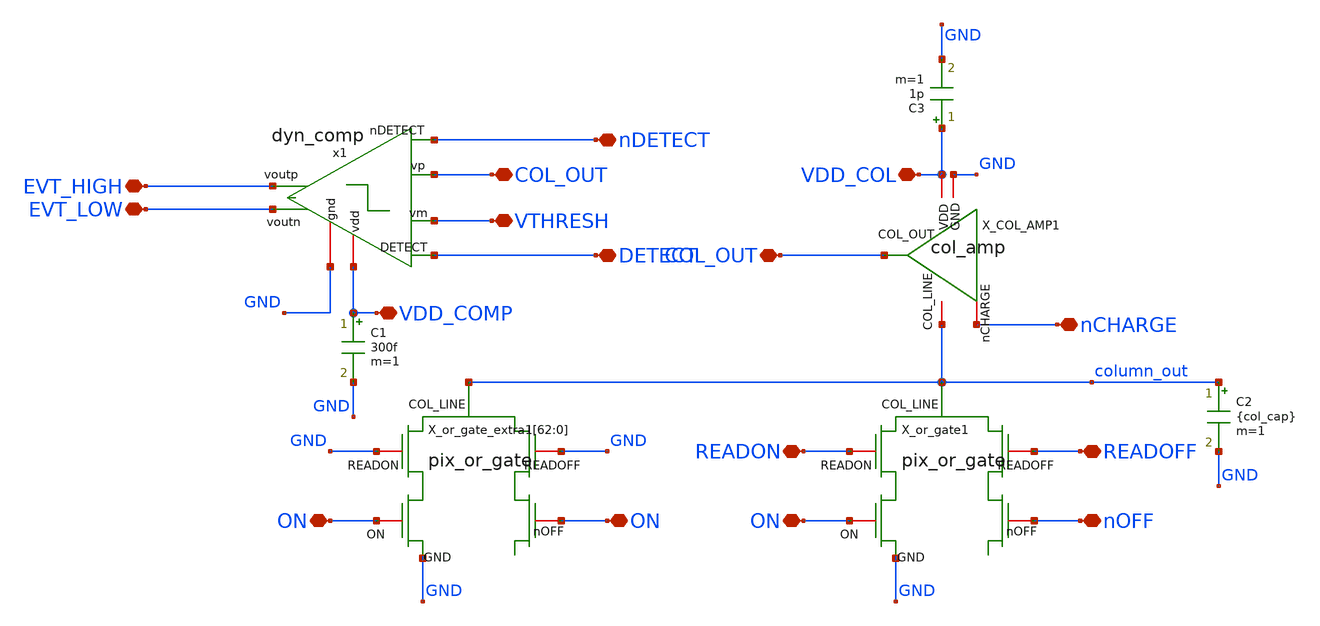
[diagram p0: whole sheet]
** sch_path: analog/xschem/col_amp_v2_std_vds/xschem/TRAN_TB_COL.sch
**.subckt TRAN_TB_COL nCHARGE nOFF READOFF ON READON VDD_COL COL_OUT ON ON DETECT VTHRESH VDD_COMP
*+ EVT_HIGH EVT_LOW nDETECT COL_OUT
*.iopin nCHARGE
*.iopin nOFF
*.iopin READOFF
*.iopin ON
*.iopin READON
*.iopin VDD_COL
*.iopin COL_OUT
*.iopin ON
*.iopin ON
*.iopin DETECT
*.iopin VTHRESH
*.iopin VDD_COMP
*.iopin EVT_HIGH
*.iopin EVT_LOW
*.iopin nDETECT
*.iopin COL_OUT
X_COL_AMP1 VDD_COL nCHARGE COL_OUT GND column_out col_amp
C2 column_out GND {col_cap} m=1
X_or_gate1 column_out READOFF READON nOFF ON GND pix_or_gate
X_or_gate_extra1[62] column_out GND GND ON ON GND pix_or_gate
X_or_gate_extra1[61] column_out GND GND ON ON GND pix_or_gate
X_or_gate_extra1[60] column_out GND GND ON ON GND pix_or_gate
X_or_gate_extra1[59] column_out GND GND ON ON GND pix_or_gate
X_or_gate_extra1[58] column_out GND GND ON ON GND pix_or_gate
X_or_gate_extra1[57] column_out GND GND ON ON GND pix_or_gate
X_or_gate_extra1[56] column_out GND GND ON ON GND pix_or_gate
X_or_gate_extra1[55] column_out GND GND ON ON GND pix_or_gate
X_or_gate_extra1[54] column_out GND GND ON ON GND pix_or_gate
X_or_gate_extra1[53] column_out GND GND ON ON GND pix_or_gate
X_or_gate_extra1[52] column_out GND GND ON ON GND pix_or_gate
X_or_gate_extra1[51] column_out GND GND ON ON GND pix_or_gate
X_or_gate_extra1[50] column_out GND GND ON ON GND pix_or_gate
X_or_gate_extra1[49] column_out GND GND ON ON GND pix_or_gate
X_or_gate_extra1[48] column_out GND GND ON ON GND pix_or_gate
X_or_gate_extra1[47] column_out GND GND ON ON GND pix_or_gate
X_or_gate_extra1[46] column_out GND GND ON ON GND pix_or_gate
X_or_gate_extra1[45] column_out GND GND ON ON GND pix_or_gate
X_or_gate_extra1[44] column_out GND GND ON ON GND pix_or_gate
X_or_gate_extra1[43] column_out GND GND ON ON GND pix_or_gate
X_or_gate_extra1[42] column_out GND GND ON ON GND pix_or_gate
X_or_gate_extra1[41] column_out GND GND ON ON GND pix_or_gate
X_or_gate_extra1[40] column_out GND GND ON ON GND pix_or_gate
X_or_gate_extra1[39] column_out GND GND ON ON GND pix_or_gate
X_or_gate_extra1[38] column_out GND GND ON ON GND pix_or_gate
X_or_gate_extra1[37] column_out GND GND ON ON GND pix_or_gate
X_or_gate_extra1[36] column_out GND GND ON ON GND pix_or_gate
X_or_gate_extra1[35] column_out GND GND ON ON GND pix_or_gate
X_or_gate_extra1[34] column_out GND GND ON ON GND pix_or_gate
X_or_gate_extra1[33] column_out GND GND ON ON GND pix_or_gate
X_or_gate_extra1[32] column_out GND GND ON ON GND pix_or_gate
X_or_gate_extra1[31] column_out GND GND ON ON GND pix_or_gate
X_or_gate_extra1[30] column_out GND GND ON ON GND pix_or_gate
X_or_gate_extra1[29] column_out GND GND ON ON GND pix_or_gate
X_or_gate_extra1[28] column_out GND GND ON ON GND pix_or_gate
X_or_gate_extra1[27] column_out GND GND ON ON GND pix_or_gate
X_or_gate_extra1[26] column_out GND GND ON ON GND pix_or_gate
X_or_gate_extra1[25] column_out GND GND ON ON GND pix_or_gate
X_or_gate_extra1[24] column_out GND GND ON ON GND pix_or_gate
X_or_gate_extra1[23] column_out GND GND ON ON GND pix_or_gate
X_or_gate_extra1[22] column_out GND GND ON ON GND pix_or_gate
X_or_gate_extra1[21] column_out GND GND ON ON GND pix_or_gate
X_or_gate_extra1[20] column_out GND GND ON ON GND pix_or_gate
X_or_gate_extra1[19] column_out GND GND ON ON GND pix_or_gate
X_or_gate_extra1[18] column_out GND GND ON ON GND pix_or_gate
X_or_gate_extra1[17] column_out GND GND ON ON GND pix_or_gate
X_or_gate_extra1[16] column_out GND GND ON ON GND pix_or_gate
X_or_gate_extra1[15] column_out GND GND ON ON GND pix_or_gate
X_or_gate_extra1[14] column_out GND GND ON ON GND pix_or_gate
X_or_gate_extra1[13] column_out GND GND ON ON GND pix_or_gate
X_or_gate_extra1[12] column_out GND GND ON ON GND pix_or_gate
X_or_gate_extra1[11] column_out GND GND ON ON GND pix_or_gate
X_or_gate_extra1[10] column_out GND GND ON ON GND pix_or_gate
X_or_gate_extra1[9] column_out GND GND ON ON GND pix_or_gate
X_or_gate_extra1[8] column_out GND GND ON ON GND pix_or_gate
X_or_gate_extra1[7] column_out GND GND ON ON GND pix_or_gate
X_or_gate_extra1[6] column_out GND GND ON ON GND pix_or_gate
X_or_gate_extra1[5] column_out GND GND ON ON GND pix_or_gate
X_or_gate_extra1[4] column_out GND GND ON ON GND pix_or_gate
X_or_gate_extra1[3] column_out GND GND ON ON GND pix_or_gate
X_or_gate_extra1[2] column_out GND GND ON ON GND pix_or_gate
X_or_gate_extra1[1] column_out GND GND ON ON GND pix_or_gate
X_or_gate_extra1[0] column_out GND GND ON ON GND pix_or_gate
x1 VDD_COMP COL_OUT VTHRESH GND nDETECT DETECT EVT_HIGH EVT_LOW dyn_comp
C1 VDD_COMP GND 300f m=1
C3 VDD_COL GND 1p m=1
**** begin user architecture code


.lib /home/alienfalcon/.ciel/sky130B/libs.tech/combined/sky130.lib.spice tt
.include /home/alienfalcon/Projects/skywater/open_dvs_py312/open_dvs/dvs_2026/col_amp/xschem/read_row8.sp

.option rshunt=1000T
.option trtol=7 abstol=1p chgtol=4e-16 vntol=1e-6 reltol=1e-4
.option temp=27

.GLOBAL VDD_COMP
.GLOBAL VDD_COL
.GLOBAL GND
.GLOBAL Reset

.param vdd = 1.8 	//supply voltage
.param tr = 1n		//rise time of voltage source signals
.param tf = 1n		//fall time of voltage source signals
.param pw = 70n		//pulse width
.param pw_chrg = 70n	//pulse width for ncharge signal
.param pw_rd = 220n	//pulse width for read signal
.param pw_det = 70n
.param pw_del = 70n	//setup and hold delays for pulses
.param pw_ld = 70n	//hold delay for latch for async
.param thresh = 1.05	//threshold voltage for comparator
.param col_cap = 300f	//column line capacitance

.param read_time = {2*pw_chrg + 2*pw_rd + 6*pw_del}

V_VDD VDD GND DC {vdd}
V_VDD_COL VDD_COL GND DC {vdd}
V_VDD_COMP VDD_COMP GND DC {vdd}
V_ON ON GND DC {vdd-0.2}
V_nOFF nOFF GND DC 0.2
V_THRESH VTHRESH GND DC {thresh}
E_nDETECT nDETECT VDD DETECT GND -1
E_RESET Reset VDD nCHARGE GND -1

V_READON READOFF GND pulse(0 {vdd} {2*pw_chrg + 4*pw_del + pw_rd} {tr} {tf} {pw_det+pw_del} {read_time})
V_READOFF READON GND pulse(0 {vdd} {pw_chrg + pw_del} {tr} {tf} {pw_det+pw_del} {read_time})

V_nCHARGE nCHARGE GND pulse({vdd} 0 0 {tr} {tf} {pw_chrg} {read_time/2})
V_DETECT DETECT GND pulse(0 {vdd} {pw_chrg + 2*pw_del} {tr} {tf} {pw_det} {read_time/2})
V_LATCH L_r GND pulse(0 {vdd} {pw_chrg+ 2*pw_del + pw_ld} {tr} {tf} {pw_det-pw_ld} {read_time/2})


.control
	save v(column_out) v(nCHARGE) v(COL_OUT) v(ON) v(nOFF) v(READON) v(READOFF) v(DETECT)
	save v(EVT_HIGH) v(EVT_LOW) v(VTHRESH)
	save v(L_a) v(L_r) v(R_r) v(R_a) v(Reset)
	save v(R_d[0]) v(R_d[1]) v(R_d[2]) v(R_d[3]) v(R_d[4]) v(R_d[5]) v(R_d[6]) v(R_d[7]) v(R_d[8])
	save i(V_VDD_COL) i(V_VDD_COMP)
	save nosub nointernals

	tran 1n 2u uic
	let Vc_max = 0
	let Vc_min = 0
	let tr_col_out = 0
	let tf_col_out = 0
	let tset_col_low = 0
	let tset_col_high = 0

	*meas tran Vc_max FIND v(COL_OUT) AT=1.3u
	*meas tran Vc_min FIND v(COL_OUT) AT=0.3u

	*let V_diff = Vc_max - Vc_min
	*let Vc_10 = V_diff*0.1 + Vc_min
	*let Vc_90 = V_diff*0.9 + Vc_min
	*let Vc_set_low = Vc_max*0.98
	*let Vc_set_high = Vc_max*1.02

	*meas tran tr_col_out TRIG v(COL_OUT) VAL=Vc_10 CROSS=1 TARG v(COL_OUT) VAL=Vc_90 CROSS=1
	*meas tran tf_col_out TRIG v(COL_OUT) VAL=Vc_90 CROSS=2 TARG v(COL_OUT) VAL=Vc_10 CROSS=2
	*meas tran tset_col_low WHEN v(COL_OUT)=Vc_set_low RISE=LAST
	*meas tran tset_col_high WHEN v(COL_OUT)=Vc_set_high FALL=LAST

	*print Vc_max Vc_min
	*print tr_col_out tf_col_out tset_col_low tset_col_high

	*save tr_col_out tf_col_out tset_col_low tset_col_high

	write TRAN_TB_COL.raw
.endc




**** end user architecture code
**.ends
.end
